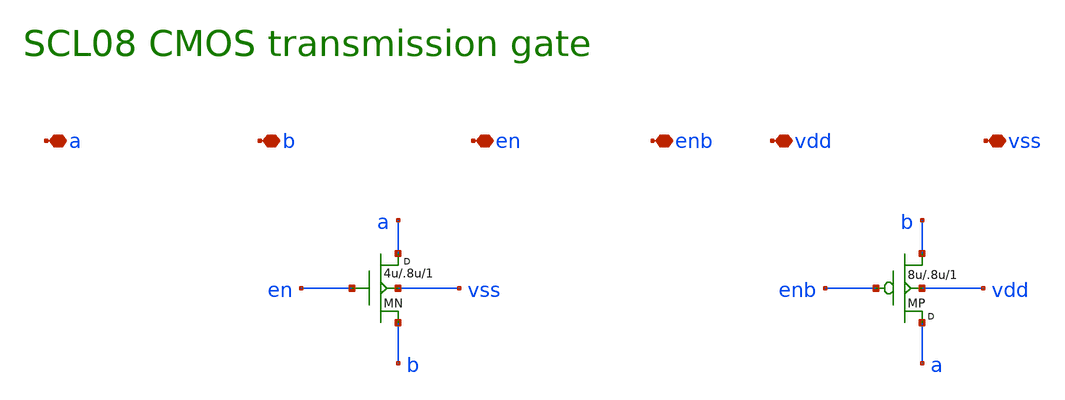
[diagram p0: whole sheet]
** sch_path: ICMC/schematic/icm_tg08.sch
**.subckt icm_tg08 a b en enb vdd vss
*.iopin a
*.iopin b
*.iopin en
*.iopin enb
*.iopin vdd
*.iopin vss
MN a en b vss N w=4u l=.8u ad=18p as=18p pd=17u ps=17u m=1
MP a enb b vdd P w=8u l=.8u ad=36p as=36p pd=25u ps=25u m=1
**.ends
.end
